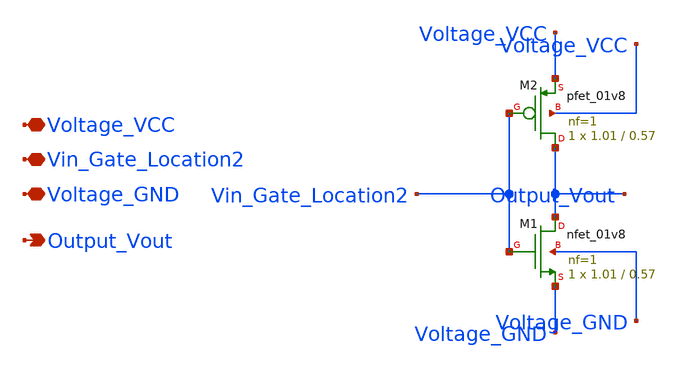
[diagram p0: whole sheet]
** sch_path: XschemRelatedFiles/MyCMOSInv.sch
**.subckt MyCMOSInv Voltage_VCC Vin_Gate_Location2 Voltage_GND Output_Vout
*.iopin Voltage_VCC
*.iopin Vin_Gate_Location2
*.iopin Voltage_GND
*.opin Output_Vout
XM1 Output_Vout Vin_Gate_Location2 Voltage_GND Voltage_GND sky130_fd_pr__nfet_01v8 L=0.57 W=1.01 nf=1
+ ad='int((1 + 1)/2) * 1.01 / 1 * 0.29' as='int((1 + 2)/2) * 1.01 / 1 * 0.29' pd='2*int((1 + 1)/2) * (1.01 / 1 + 0.29)'
+ ps='2*int((1 + 2)/2) * (1.01 / 1 + 0.29)' nrd='0.29 / 1.01 ' nrs='0.29 / 1.01 ' sa=0 sb=0 sd=0 mult=1
+ m=1
XM2 Output_Vout Vin_Gate_Location2 Voltage_VCC Voltage_VCC sky130_fd_pr__pfet_01v8 L=0.57 W=1.01 nf=1
+ ad='int((1 + 1)/2) * 1.01 / 1 * 0.29' as='int((1 + 2)/2) * 1.01 / 1 * 0.29' pd='2*int((1 + 1)/2) * (1.01 / 1 + 0.29)'
+ ps='2*int((1 + 2)/2) * (1.01 / 1 + 0.29)' nrd='0.29 / 1.01 ' nrs='0.29 / 1.01 ' sa=0 sb=0 sd=0 mult=1
+ m=1
**.ends
.end
